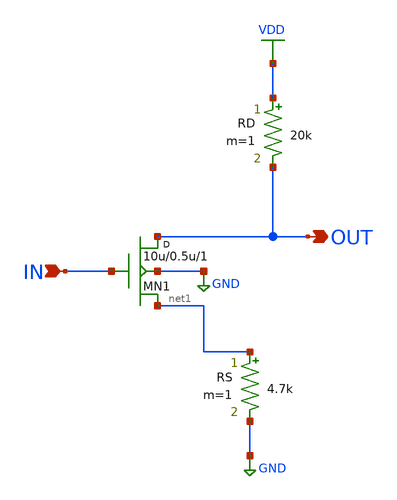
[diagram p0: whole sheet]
** sch_path: E3_238_Analog_VLSI_Circuits/09_Source_Degeneration/cs_source_degenerated.sch
**.subckt cs_source_degenerated IN OUT
*.ipin IN
*.opin OUT
MN1 OUT IN net1 GND nmos w=10u l=0.5u m=1
RD VDD OUT 20k m=1
RS net1 GND 4.7k m=1
**** begin user architecture code

.include /home/anirudh/Analog_VLSI_Projects/models/cmos_180nm.mod
VDD VDD 0 DC 1.8
VIN IN 0 DC 0.8 AC 1
CL OUT GND 1p

.control
  op
  print v(OUT)
  ac dec 20 1 1G
  plot db(v(OUT))
  plot phase(v(OUT))*180/pi
.endc


**** end user architecture code
**.ends
.GLOBAL VDD
.GLOBAL GND
.end
